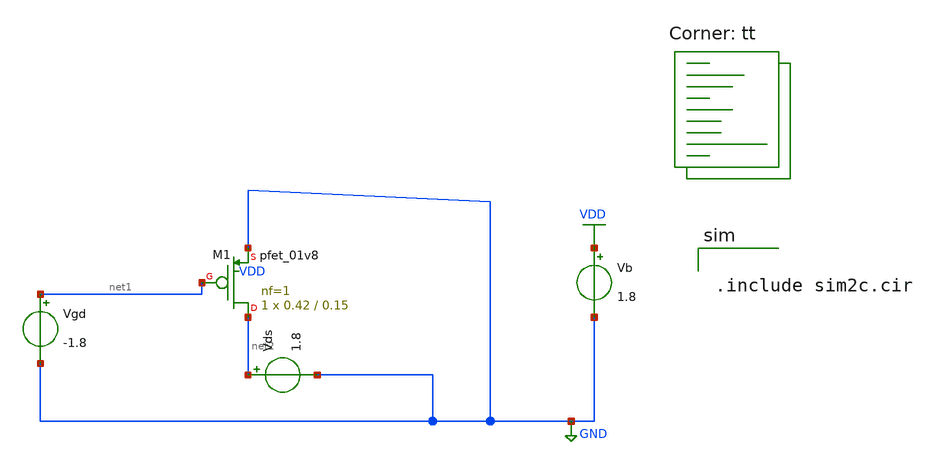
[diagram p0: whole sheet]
** sch_path: assignments/assignment1/assign2c.sch
**.subckt assign2c
Vgd net1 GND -1.8
Vds net2 GND 1.8
XM1 net2 net1 GND VDD sky130_fd_pr__pfet_01v8 L=0.15 W=0.42 nf=1 ad='int((nf+1)/2) * W/nf * 0.29' as='int((nf+2)/2) * W/nf * 0.29'
+ pd='2*int((nf+1)/2) * (W/nf + 0.29)' ps='2*int((nf+2)/2) * (W/nf + 0.29)' nrd='0.29 / W' nrs='0.29 / W'
+ sa=0 sb=0 sd=0 mult=1 m=1
Vb VDD GND 1.8
**** begin user architecture code
.lib $::SKYWATER_MODELS/sky130.lib.spice tt


.include sim2c.cir


**** end user architecture code
**.ends
.GLOBAL GND
.GLOBAL VDD
.end
